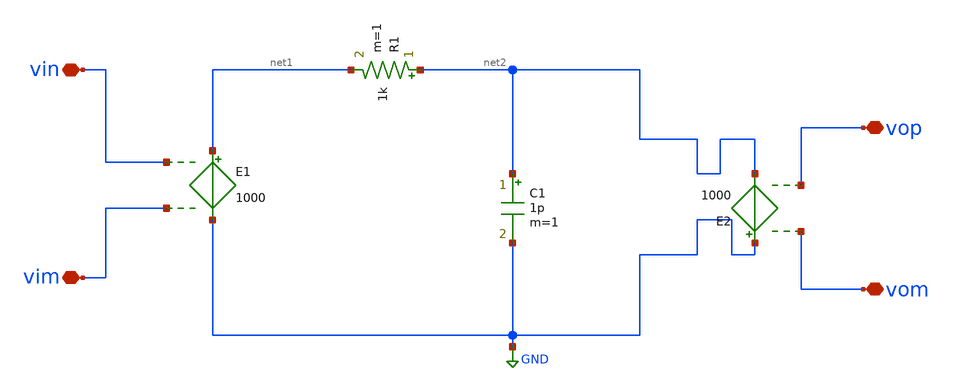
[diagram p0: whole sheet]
** sch_path: xschem/untitled-4.sch
**.subckt untitled-4 vop vom vin vim
*.iopin vop
*.iopin vom
*.iopin vin
*.iopin vim
E1 net1 GND vin vim 1000
R1 net2 net1 1k m=1
C1 net2 GND 1p m=1
E2 GND net2 vom vop 1000
**.ends
.GLOBAL GND
.end
